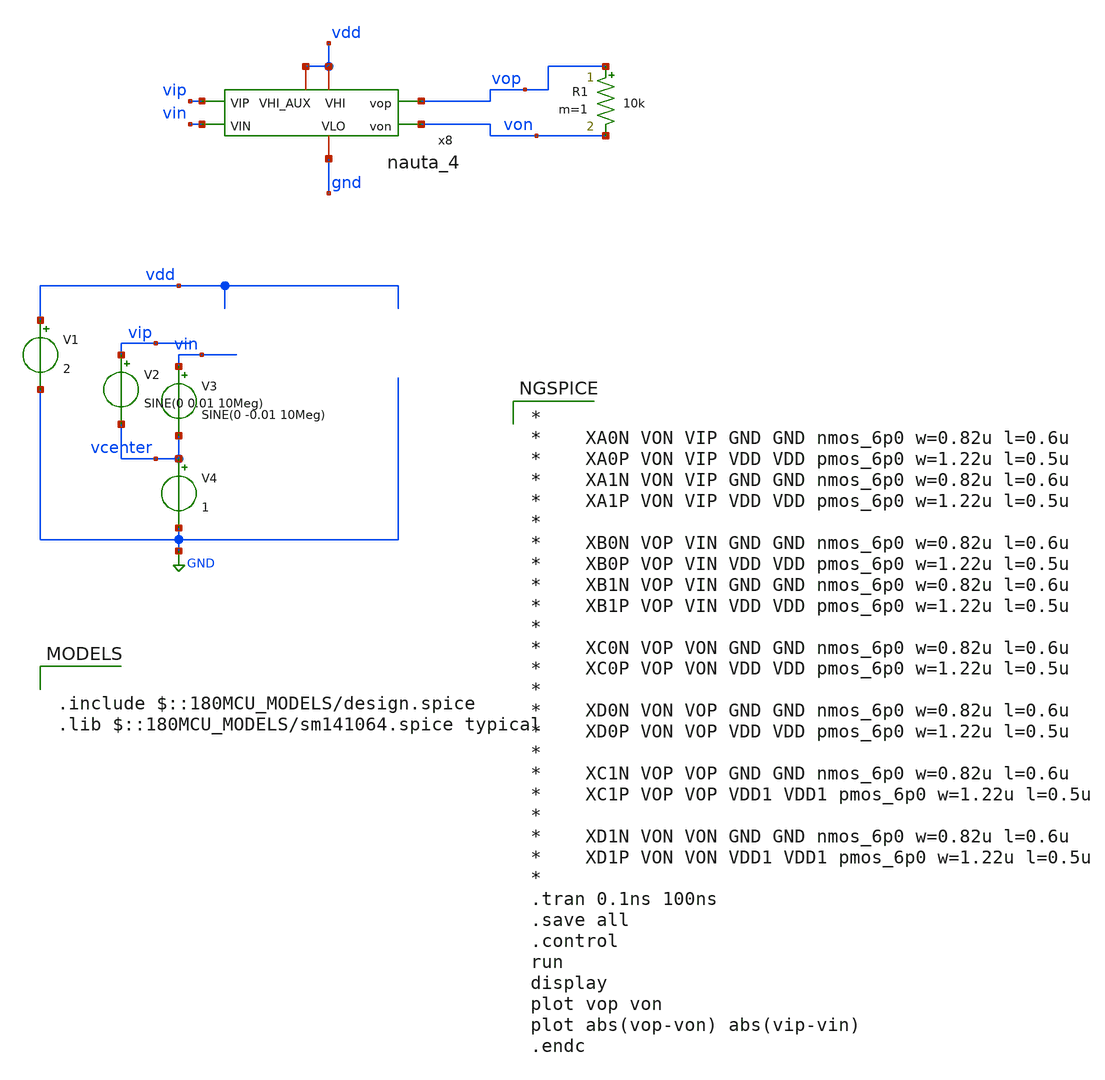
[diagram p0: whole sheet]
** sch_path: xschem/nauta_test.sch
**.subckt nauta_test
V1 vdd GND 2
V2 vip vcenter SINE(0 0.01 10Meg)
V3 vin vcenter SINE(0 -0.01 10Meg)
V4 vcenter GND 1
R1 vop von 10k m=1
x8 vdd vdd vip vop vin von gnd nauta_4
**** begin user architecture code

.include $::180MCU_MODELS/design.spice
.lib $::180MCU_MODELS/sm141064.spice typical


*
*	XA0N VON VIP GND GND nmos_6p0 w=0.82u l=0.6u
*	XA0P VON VIP VDD VDD pmos_6p0 w=1.22u l=0.5u
*	XA1N VON VIP GND GND nmos_6p0 w=0.82u l=0.6u
*	XA1P VON VIP VDD VDD pmos_6p0 w=1.22u l=0.5u
*
*	XB0N VOP VIN GND GND nmos_6p0 w=0.82u l=0.6u
*	XB0P VOP VIN VDD VDD pmos_6p0 w=1.22u l=0.5u
*	XB1N VOP VIN GND GND nmos_6p0 w=0.82u l=0.6u
*	XB1P VOP VIN VDD VDD pmos_6p0 w=1.22u l=0.5u
*
*	XC0N VOP VON GND GND nmos_6p0 w=0.82u l=0.6u
*	XC0P VOP VON VDD VDD pmos_6p0 w=1.22u l=0.5u
*
*	XD0N VON VOP GND GND nmos_6p0 w=0.82u l=0.6u
*	XD0P VON VOP VDD VDD pmos_6p0 w=1.22u l=0.5u
*
*	XC1N VOP VOP GND GND nmos_6p0 w=0.82u l=0.6u
*	XC1P VOP VOP VDD1 VDD1 pmos_6p0 w=1.22u l=0.5u
*
*	XD1N VON VON GND GND nmos_6p0 w=0.82u l=0.6u
*	XD1P VON VON VDD1 VDD1 pmos_6p0 w=1.22u l=0.5u
*
.tran 0.1ns 100ns
.save all
.control
run
display
plot vop von
plot abs(vop-von) abs(vip-vin)
.endc


**** end user architecture code
**.ends

* expanding   symbol:  nauta_4.sym # of pins=7
** sym_path: xschem/nauta_4.sym
** sch_path: xschem/nauta_4.sch
.subckt nauta_4 VHI_AUX VHI VIP vop VIN von VLO
*.ipin VIP
*.ipin VIN
*.opin vop
*.opin von
*.iopin VHI
*.iopin VHI_AUX
*.iopin VLO
**** begin user architecture code

.subckt NAUTA VOP VON VIP VIN VHI VHI_AUX VLO

XA0N VON VIP VLO VLO nmos_6p0 w=0.82u l=0.6u
XA0P VON VIP VHI VHI pmos_6p0 w=1.22u l=0.5u
XA1N VON VIP VLO VLO nmos_6p0 w=0.82u l=0.6u
XA1P VON VIP VHI VHI pmos_6p0 w=1.22u l=0.5u

XB0N VOP VIN VLO VLO nmos_6p0 w=0.82u l=0.6u
XB0P VOP VIN VHI VHI pmos_6p0 w=1.22u l=0.5u
XB1N VOP VIN VLO VLO nmos_6p0 w=0.82u l=0.6u
XB1P VOP VIN VHI VHI pmos_6p0 w=1.22u l=0.5u

XC0N VOP VON VLO VLO nmos_6p0 w=0.82u l=0.6u
XC0P VOP VON VHI VHI pmos_6p0 w=1.22u l=0.5u

XD0N VON VOP VLO VLO nmos_6p0 w=0.82u l=0.6u
XD0P VON VOP VHI VHI pmos_6p0 w=1.22u l=0.5u

XC1N VOP VOP VLO VLO nmos_6p0 w=0.82u l=0.6u
XC1P VOP VOP VHI_AUX VHI_AUX pmos_6p0 w=1.22u l=0.5u

XD1N VON VON VLO VLO nmos_6p0 w=0.82u l=0.6u
XD1P VON VON VHI_AUX VHI_AUX pmos_6p0 w=1.22u l=0.5u

.ends

XDUT VOP VON VIP VIN VHI VHI_AUX VLO NAUTA


**** end user architecture code
.ends

.GLOBAL GND
.end
